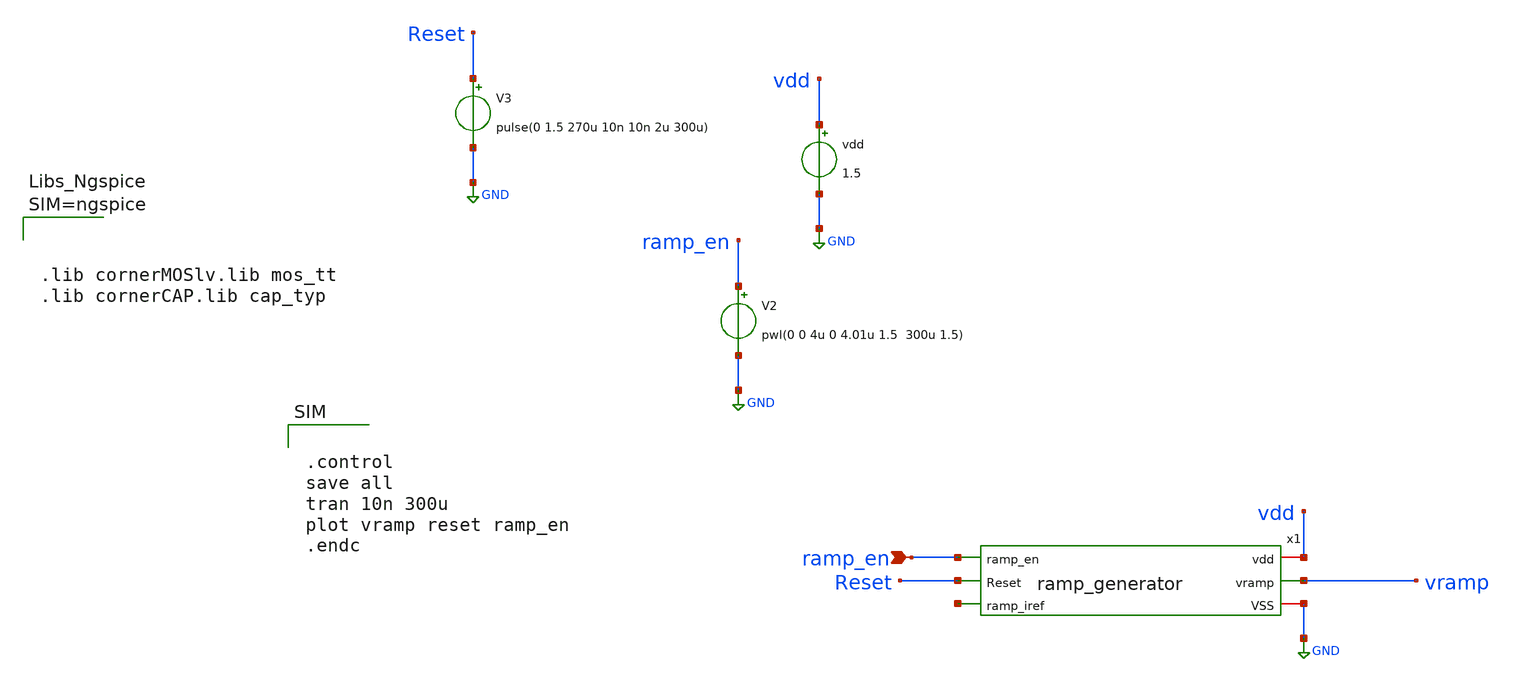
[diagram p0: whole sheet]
** sch_path: dependencies/ADC/dependencies/RAMP_GEN/RAMP_GEN-main/testbenches/tran/xschem/tb_ramp_generator.sch
**.subckt tb_ramp_generator ramp_en
*.ipin ramp_en
vdd vdd GND 1.5
V2 ramp_en GND pwl(0 0 4u 0 4.01u 1.5 300u 1.5)
V3 Reset GND pulse(0 1.5 270u 10n 10n 2u 300u)
x1 vdd ramp_en vramp Reset GND net1 Nbulk Pbulk ramp_generator
**** begin user architecture code




.lib cornerMOSlv.lib mos_tt
.lib cornerCAP.lib cap_typ






.control
save all
tran 10n 300u
plot vramp reset ramp_en
.endc



**** end user architecture code
**.ends
.GLOBAL GND
.end
